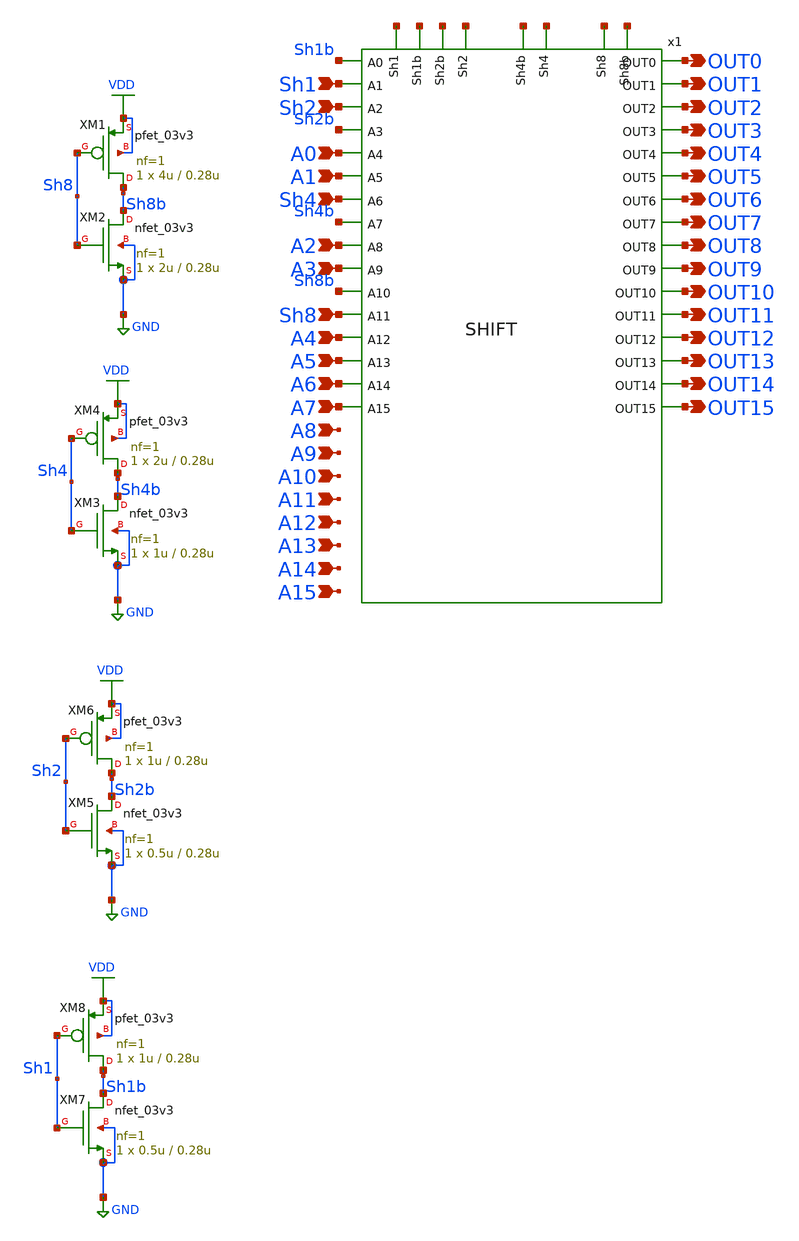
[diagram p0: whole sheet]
** sch_path: SHIFT_INVERTERS.sch
**.subckt SHIFT_INVERTERS OUT0 OUT1 OUT2 OUT3 OUT4 OUT5 OUT6 OUT7 OUT8 OUT9 OUT10 OUT11 OUT12 OUT13
*+ OUT14 OUT15 A0 A1 A2 A3 A4 A5 A6 A7 A8 A9 A10 A11 A12 A13 A14 A15 Sh1 Sh2 Sh4 Sh8
*.opin OUT0
*.opin OUT1
*.opin OUT2
*.opin OUT3
*.opin OUT4
*.opin OUT5
*.opin OUT6
*.opin OUT7
*.opin OUT8
*.opin OUT9
*.opin OUT10
*.opin OUT11
*.opin OUT12
*.opin OUT13
*.opin OUT14
*.opin OUT15
*.ipin A0
*.ipin A1
*.ipin A2
*.ipin A3
*.ipin A4
*.ipin A5
*.ipin A6
*.ipin A7
*.ipin A8
*.ipin A9
*.ipin A10
*.ipin A11
*.ipin A12
*.ipin A13
*.ipin A14
*.ipin A15
*.ipin Sh1
*.ipin Sh2
*.ipin Sh4
*.ipin Sh8
x1 net1 net2 net3 net4 Sh1b OUT0 Sh1 OUT1 net5 net6 Sh2 OUT2 Sh2b OUT3 net7 net8 OUT4 A0 OUT5 A1
+ OUT6 Sh4 OUT7 Sh4b OUT8 A2 A3 OUT9 Sh8b OUT10 OUT11 Sh8 OUT12 A4 A5 OUT13 OUT14 A6 OUT15 A7 SHIFT
XM2 Sh8b Sh8 GND GND nfet_03v3 L=0.28u W=2u nf=1 ad='int((nf+1)/2) * W/nf * 0.18u' as='int((nf+2)/2) * W/nf * 0.18u'
+ pd='2*int((nf+1)/2) * (W/nf + 0.18u)' ps='2*int((nf+2)/2) * (W/nf + 0.18u)' nrd='0.18u / W' nrs='0.18u / W'
+ sa=0 sb=0 sd=0 m=1
XM1 Sh8b Sh8 VDD VDD pfet_03v3 L=0.28u W=4u nf=1 ad='int((nf+1)/2) * W/nf * 0.18u' as='int((nf+2)/2) * W/nf * 0.18u'
+ pd='2*int((nf+1)/2) * (W/nf + 0.18u)' ps='2*int((nf+2)/2) * (W/nf + 0.18u)' nrd='0.18u / W' nrs='0.18u / W'
+ sa=0 sb=0 sd=0 m=1
XM3 Sh4b Sh4 GND GND nfet_03v3 L=0.28u W=1u nf=1 ad='int((nf+1)/2) * W/nf * 0.18u' as='int((nf+2)/2) * W/nf * 0.18u'
+ pd='2*int((nf+1)/2) * (W/nf + 0.18u)' ps='2*int((nf+2)/2) * (W/nf + 0.18u)' nrd='0.18u / W' nrs='0.18u / W'
+ sa=0 sb=0 sd=0 m=1
XM4 Sh4b Sh4 VDD VDD pfet_03v3 L=0.28u W=2u nf=1 ad='int((nf+1)/2) * W/nf * 0.18u' as='int((nf+2)/2) * W/nf * 0.18u'
+ pd='2*int((nf+1)/2) * (W/nf + 0.18u)' ps='2*int((nf+2)/2) * (W/nf + 0.18u)' nrd='0.18u / W' nrs='0.18u / W'
+ sa=0 sb=0 sd=0 m=1
XM5 Sh2b Sh2 GND GND nfet_03v3 L=0.28u W=0.5u nf=1 ad='int((nf+1)/2) * W/nf * 0.18u' as='int((nf+2)/2) * W/nf * 0.18u'
+ pd='2*int((nf+1)/2) * (W/nf + 0.18u)' ps='2*int((nf+2)/2) * (W/nf + 0.18u)' nrd='0.18u / W' nrs='0.18u / W'
+ sa=0 sb=0 sd=0 m=1
XM6 Sh2b Sh2 VDD VDD pfet_03v3 L=0.28u W=1u nf=1 ad='int((nf+1)/2) * W/nf * 0.18u' as='int((nf+2)/2) * W/nf * 0.18u'
+ pd='2*int((nf+1)/2) * (W/nf + 0.18u)' ps='2*int((nf+2)/2) * (W/nf + 0.18u)' nrd='0.18u / W' nrs='0.18u / W'
+ sa=0 sb=0 sd=0 m=1
XM7 Sh1b Sh1 GND GND nfet_03v3 L=0.28u W=0.5u nf=1 ad='int((nf+1)/2) * W/nf * 0.18u' as='int((nf+2)/2) * W/nf * 0.18u'
+ pd='2*int((nf+1)/2) * (W/nf + 0.18u)' ps='2*int((nf+2)/2) * (W/nf + 0.18u)' nrd='0.18u / W' nrs='0.18u / W'
+ sa=0 sb=0 sd=0 m=1
XM8 Sh1b Sh1 VDD VDD pfet_03v3 L=0.28u W=1u nf=1 ad='int((nf+1)/2) * W/nf * 0.18u' as='int((nf+2)/2) * W/nf * 0.18u'
+ pd='2*int((nf+1)/2) * (W/nf + 0.18u)' ps='2*int((nf+2)/2) * (W/nf + 0.18u)' nrd='0.18u / W' nrs='0.18u / W'
+ sa=0 sb=0 sd=0 m=1
**.ends
.GLOBAL GND
.GLOBAL VDD
.end
